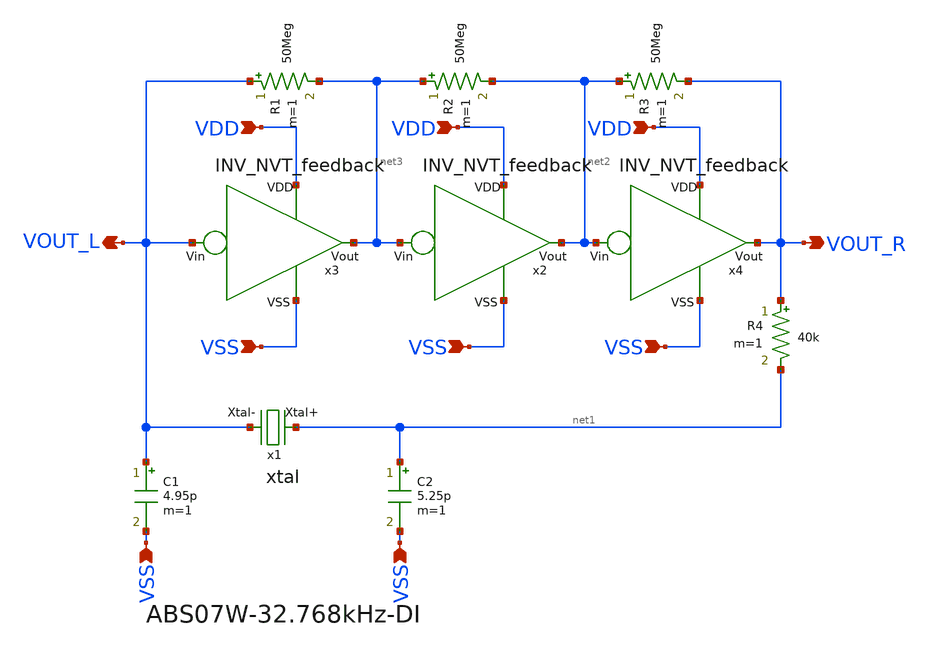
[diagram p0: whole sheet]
** sch_path: design/THESIS_EXP_RO_INVERTER_SKY130A/xtal_osc.sch
**.subckt xtal_osc VSS VSS VOUT_R VOUT_L VDD VSS VDD VDD VSS VSS
*.ipin VSS
*.ipin VSS
*.opin VOUT_R
*.opin VOUT_L
*.ipin VDD
*.ipin VSS
*.ipin VDD
*.ipin VDD
*.ipin VSS
*.ipin VSS
x1 net1 VOUT_L xtal
C1 VOUT_L VSS 4.95p m=1
C2 net1 VSS 5.25p m=1
R1 VOUT_L net3 50Meg m=1
x4 VDD VSS VOUT_R net2 INV_NVT_feedback
R2 net3 net2 50Meg m=1
R3 net2 VOUT_R 50Meg m=1
R4 VOUT_R net1 40k m=1
x2 VDD VSS net2 net3 INV_NVT_feedback
x3 VDD VSS net3 VOUT_L INV_NVT_feedback
**.ends

* expanding   symbol:  THESIS_EXP_RO_INVERTER_SKY130A/xtal.sym # of pins=2
** sym_path: design/THESIS_EXP_RO_INVERTER_SKY130A/xtal.sym
** sch_path: design/THESIS_EXP_RO_INVERTER_SKY130A/xtal.sch
.subckt xtal Xtal+ Xtal-
*.iopin Xtal+
*.iopin Xtal-
R1 Xtal+ net1 38.194k m=1
C1 net1 net2 4.68f m=1
L1 net2 Xtal- 5048.571 m=1
C2 Xtal+ Xtal- 1.15p m=1
.ends


* expanding   symbol:  THESIS_EXP_RO_INVERTER_SKY130A/INV_NVT_feedback.sym # of pins=4
** sym_path: design/THESIS_EXP_RO_INVERTER_SKY130A/INV_NVT_feedback.sym
** sch_path: design/THESIS_EXP_RO_INVERTER_SKY130A/INV_NVT_feedback.sch
.subckt INV_NVT_feedback VDD VSS Vout Vin
*.ipin VSS
*.ipin Vin
*.opin Vout
*.ipin VDD
XM1 net4 Vin VDD VDD sky130_fd_pr__pfet_01v8_lvt L=0.35 W=7 nf=1 ad='int((nf+1)/2) * W/nf * 0.29' as='int((nf+2)/2) * W/nf * 0.29'
+ pd='2*int((nf+1)/2) * (W/nf + 0.29)' ps='2*int((nf+2)/2) * (W/nf + 0.29)' nrd='0.29 / W' nrs='0.29 / W'
+ sa=0 sb=0 sd=0 mult=m_alpha m=m_alpha
XM2 net1 Vin vn VSS sky130_fd_pr__nfet_03v3_nvt L=0.6 W=1 nf=1 ad='int((nf+1)/2) * W/nf * 0.29' as='int((nf+2)/2) * W/nf * 0.29'
+ pd='2*int((nf+1)/2) * (W/nf + 0.29)' ps='2*int((nf+2)/2) * (W/nf + 0.29)' nrd='0.29 / W' nrs='0.29 / W'
+ sa=0 sb=0 sd=0 mult=m_beta m=m_beta
XM3 net2 Vin VSS VSS sky130_fd_pr__nfet_03v3_nvt L=0.6 W=1 nf=1 ad='int((nf+1)/2) * W/nf * 0.29' as='int((nf+2)/2) * W/nf * 0.29'
+ pd='2*int((nf+1)/2) * (W/nf + 0.29)' ps='2*int((nf+2)/2) * (W/nf + 0.29)' nrd='0.29 / W' nrs='0.29 / W'
+ sa=0 sb=0 sd=0 mult=m_I0 m=m_I0
XM4 VDD Vout net3 VSS sky130_fd_pr__nfet_03v3_nvt L=0.6 W=1 nf=1 ad='int((nf+1)/2) * W/nf * 0.29' as='int((nf+2)/2) * W/nf * 0.29'
+ pd='2*int((nf+1)/2) * (W/nf + 0.29)' ps='2*int((nf+2)/2) * (W/nf + 0.29)' nrd='0.29 / W' nrs='0.29 / W'
+ sa=0 sb=0 sd=0 mult=m_gamma m=m_gamma
V1 vn net2 0
.save i(v1)
V2 Vout net1 0
.save i(v2)
V3 net3 vn 0
.save i(v3)
V4 net4 Vout 0
.save i(v4)
.ends

.end
